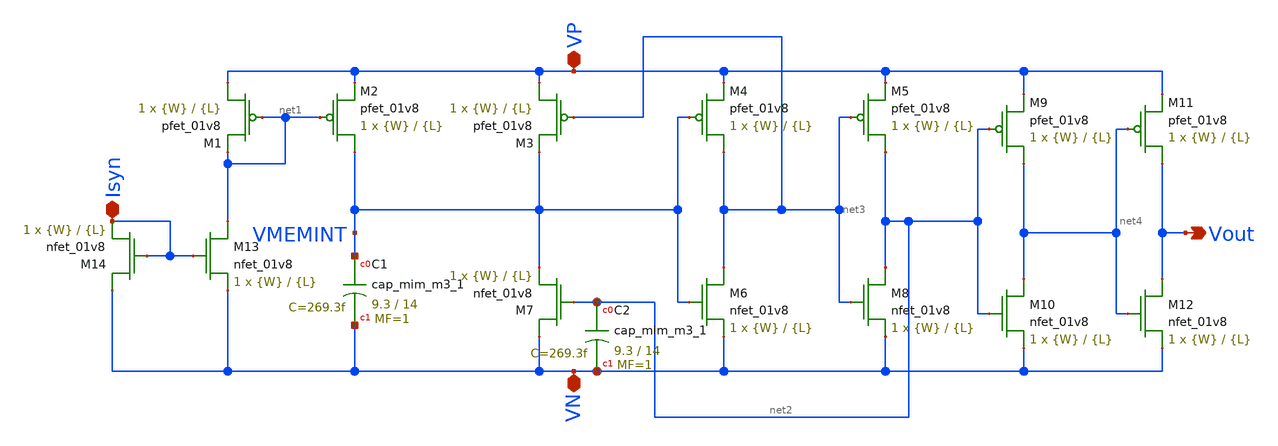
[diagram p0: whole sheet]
** sch_path: schematic/besrour_neuron_cm.sch
**.subckt besrour_neuron_cm VP VN Isyn Vout
*.iopin VP
*.iopin VN
*.iopin Isyn
*.opin Vout
XM2 VMEMINT net1 VP VDD sky130_fd_pr__pfet_01v8 L={L} W={W} nf=1 ad='int((nf+1)/2) * W/nf * 0.29' as='int((nf+2)/2) * W/nf * 0.29'
+ pd='2*int((nf+1)/2) * (W/nf + 0.29)' ps='2*int((nf+2)/2) * (W/nf + 0.29)' nrd='0.29 / W' nrs='0.29 / W'
+ sa=0 sb=0 sd=0 mult=1 m=1
XM3 VP net3 VMEMINT VDD sky130_fd_pr__pfet_01v8 L={L} W={W} nf=1 ad='int((nf+1)/2) * W/nf * 0.29' as='int((nf+2)/2) * W/nf * 0.29'
+ pd='2*int((nf+1)/2) * (W/nf + 0.29)' ps='2*int((nf+2)/2) * (W/nf + 0.29)' nrd='0.29 / W' nrs='0.29 / W'
+ sa=0 sb=0 sd=0 mult=1 m=1
XM4 net3 VMEMINT VP VDD sky130_fd_pr__pfet_01v8 L={L} W={W} nf=1 ad='int((nf+1)/2) * W/nf * 0.29' as='int((nf+2)/2) * W/nf * 0.29'
+ pd='2*int((nf+1)/2) * (W/nf + 0.29)' ps='2*int((nf+2)/2) * (W/nf + 0.29)' nrd='0.29 / W' nrs='0.29 / W'
+ sa=0 sb=0 sd=0 mult=1 m=1
XM5 net2 net3 VP VDD sky130_fd_pr__pfet_01v8 L={L} W={W} nf=1 ad='int((nf+1)/2) * W/nf * 0.29' as='int((nf+2)/2) * W/nf * 0.29'
+ pd='2*int((nf+1)/2) * (W/nf + 0.29)' ps='2*int((nf+2)/2) * (W/nf + 0.29)' nrd='0.29 / W' nrs='0.29 / W'
+ sa=0 sb=0 sd=0 mult=1 m=1
XM6 net3 VMEMINT VN GND sky130_fd_pr__nfet_01v8 L={L} W={W} nf=1 ad='int((nf+1)/2) * W/nf * 0.29' as='int((nf+2)/2) * W/nf * 0.29'
+ pd='2*int((nf+1)/2) * (W/nf + 0.29)' ps='2*int((nf+2)/2) * (W/nf + 0.29)' nrd='0.29 / W' nrs='0.29 / W'
+ sa=0 sb=0 sd=0 mult=1 m=1
XM8 net2 net3 VN GND sky130_fd_pr__nfet_01v8 L={L} W={W} nf=1 ad='int((nf+1)/2) * W/nf * 0.29' as='int((nf+2)/2) * W/nf * 0.29'
+ pd='2*int((nf+1)/2) * (W/nf + 0.29)' ps='2*int((nf+2)/2) * (W/nf + 0.29)' nrd='0.29 / W' nrs='0.29 / W'
+ sa=0 sb=0 sd=0 mult=1 m=1
XM9 net4 net2 VP VDD sky130_fd_pr__pfet_01v8 L={L} W={W} nf=1 ad='int((nf+1)/2) * W/nf * 0.29' as='int((nf+2)/2) * W/nf * 0.29'
+ pd='2*int((nf+1)/2) * (W/nf + 0.29)' ps='2*int((nf+2)/2) * (W/nf + 0.29)' nrd='0.29 / W' nrs='0.29 / W'
+ sa=0 sb=0 sd=0 mult=1 m=1
XM10 net4 net2 VN GND sky130_fd_pr__nfet_01v8 L={L} W={W} nf=1 ad='int((nf+1)/2) * W/nf * 0.29' as='int((nf+2)/2) * W/nf * 0.29'
+ pd='2*int((nf+1)/2) * (W/nf + 0.29)' ps='2*int((nf+2)/2) * (W/nf + 0.29)' nrd='0.29 / W' nrs='0.29 / W'
+ sa=0 sb=0 sd=0 mult=1 m=1
XM11 Vout net4 VP VDD sky130_fd_pr__pfet_01v8 L={L} W={W} nf=1 ad='int((nf+1)/2) * W/nf * 0.29' as='int((nf+2)/2) * W/nf * 0.29'
+ pd='2*int((nf+1)/2) * (W/nf + 0.29)' ps='2*int((nf+2)/2) * (W/nf + 0.29)' nrd='0.29 / W' nrs='0.29 / W'
+ sa=0 sb=0 sd=0 mult=1 m=1
XM12 Vout net4 VN GND sky130_fd_pr__nfet_01v8 L={L} W={W} nf=1 ad='int((nf+1)/2) * W/nf * 0.29' as='int((nf+2)/2) * W/nf * 0.29'
+ pd='2*int((nf+1)/2) * (W/nf + 0.29)' ps='2*int((nf+2)/2) * (W/nf + 0.29)' nrd='0.29 / W' nrs='0.29 / W'
+ sa=0 sb=0 sd=0 mult=1 m=1
XM13 net1 Isyn VN GND sky130_fd_pr__nfet_01v8 L={L} W={W} nf=1 ad='int((nf+1)/2) * W/nf * 0.29' as='int((nf+2)/2) * W/nf * 0.29'
+ pd='2*int((nf+1)/2) * (W/nf + 0.29)' ps='2*int((nf+2)/2) * (W/nf + 0.29)' nrd='0.29 / W' nrs='0.29 / W'
+ sa=0 sb=0 sd=0 mult=1 m=1
XM14 VN Isyn Isyn GND sky130_fd_pr__nfet_01v8 L={L} W={W} nf=1 ad='int((nf+1)/2) * W/nf * 0.29' as='int((nf+2)/2) * W/nf * 0.29'
+ pd='2*int((nf+1)/2) * (W/nf + 0.29)' ps='2*int((nf+2)/2) * (W/nf + 0.29)' nrd='0.29 / W' nrs='0.29 / W'
+ sa=0 sb=0 sd=0 mult=1 m=1
XM1 VP net1 net1 VDD sky130_fd_pr__pfet_01v8 L={L} W={W} nf=1 ad='int((nf+1)/2) * W/nf * 0.29' as='int((nf+2)/2) * W/nf * 0.29'
+ pd='2*int((nf+1)/2) * (W/nf + 0.29)' ps='2*int((nf+2)/2) * (W/nf + 0.29)' nrd='0.29 / W' nrs='0.29 / W'
+ sa=0 sb=0 sd=0 mult=1 m=1
XM7 VN net2 VMEMINT GND sky130_fd_pr__nfet_01v8 L={L} W={W} nf=1 ad='int((nf+1)/2) * W/nf * 0.29' as='int((nf+2)/2) * W/nf * 0.29'
+ pd='2*int((nf+1)/2) * (W/nf + 0.29)' ps='2*int((nf+2)/2) * (W/nf + 0.29)' nrd='0.29 / W' nrs='0.29 / W'
+ sa=0 sb=0 sd=0 mult=1 m=1
XC1 VMEMINT VN sky130_fd_pr__cap_mim_m3_1 W=9.3 L=14 MF=1 m=1
XC2 net2 VN sky130_fd_pr__cap_mim_m3_1 W=9.3 L=14 MF=1 m=1
**.ends
.end
